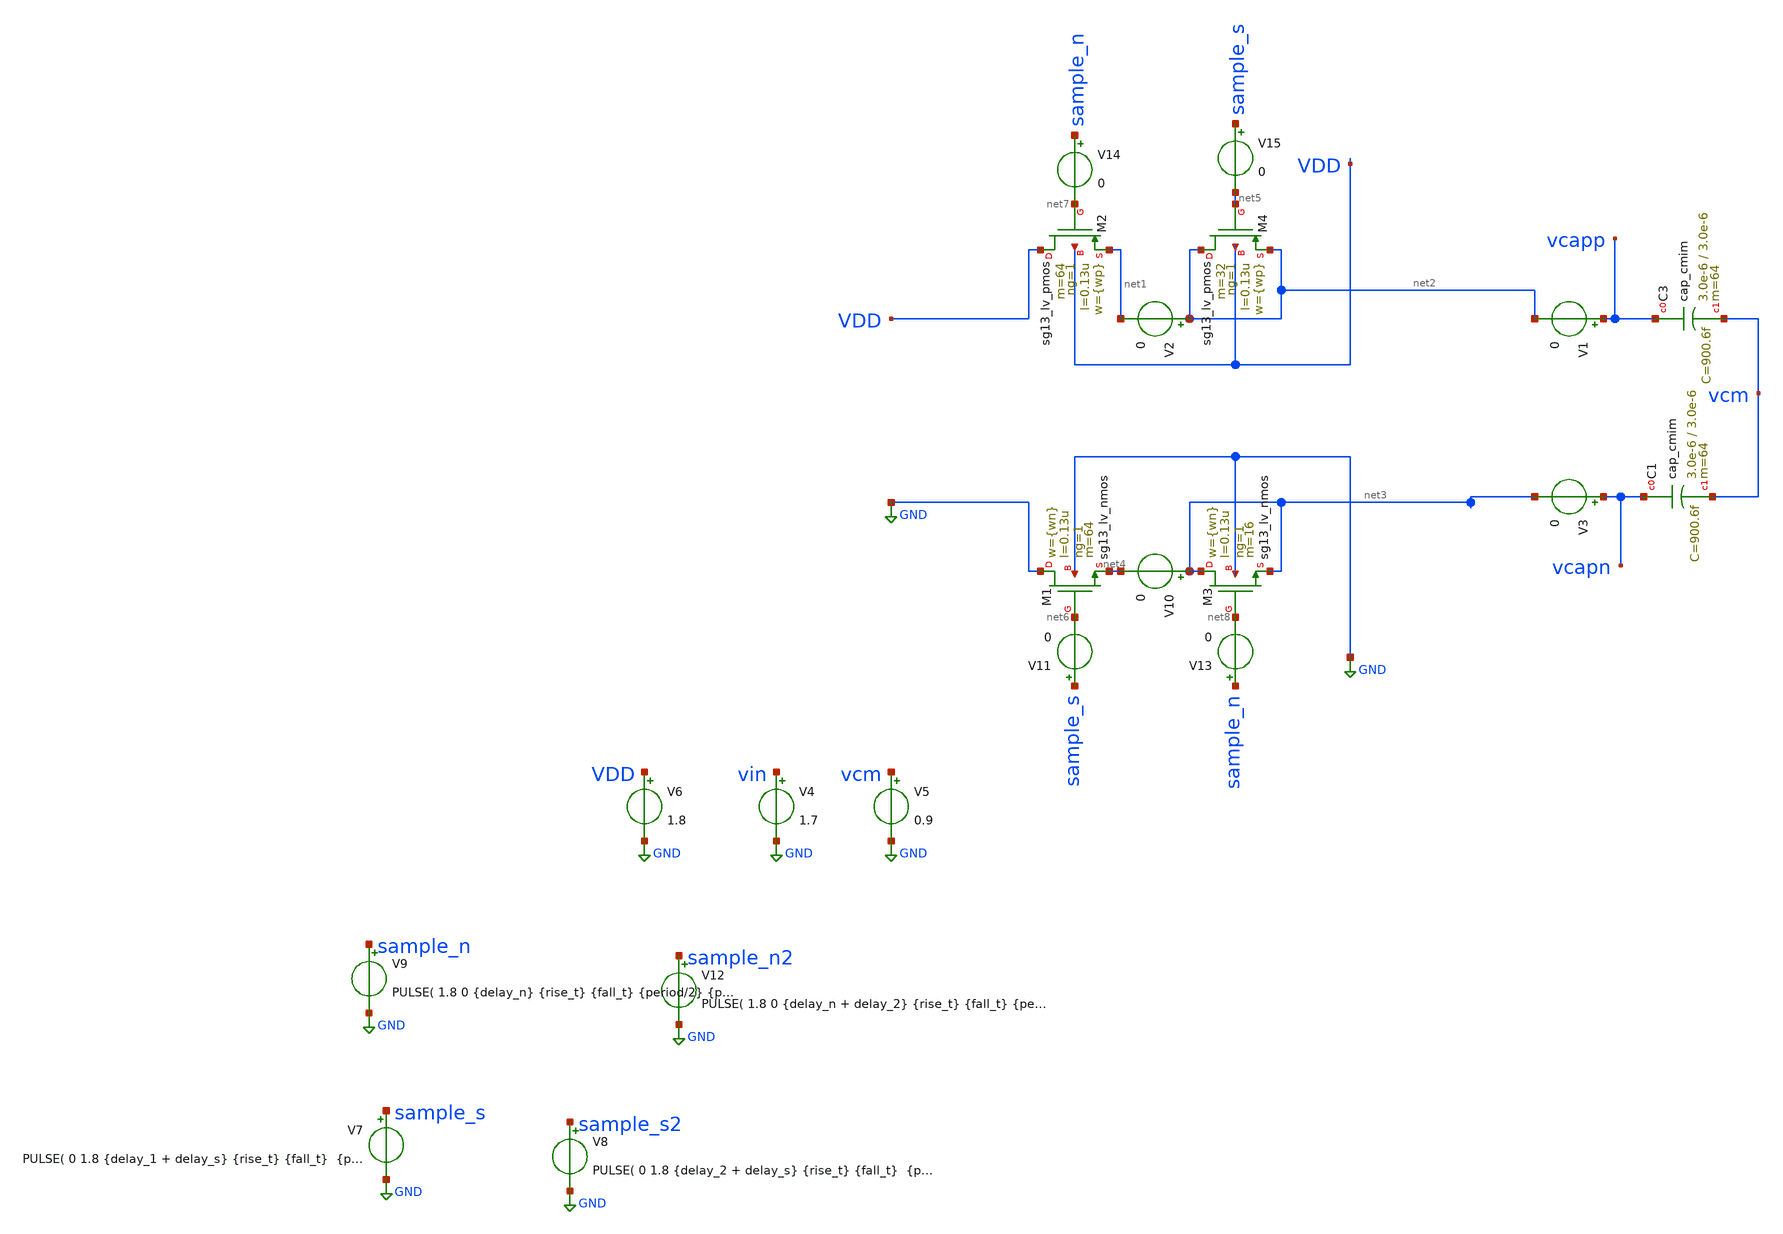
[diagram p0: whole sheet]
** sch_path: xschem/dac_icms_cell/testbenches/tb_dummy.sch
**.subckt tb_dummy
V1 vcapp net2 0
V3 vcapn net3 0
XM1 GND net6 net4 GND sg13_lv_nmos w={wn} l=0.13u ng=1 m=64 mm_ok=1
XM2 VDD net7 net1 VDD sg13_lv_pmos w={wp} l=0.13u ng=1 m=64 mm_ok=1
XM3 net3 net8 net3 GND sg13_lv_nmos w={wn} l=0.13u ng=1 m=16 mm_ok=1
XM4 net2 net5 net2 VDD sg13_lv_pmos w={wp} l=0.13u ng=1 m=32 mm_ok=1
V4 vin GND 1.7
V5 vcm GND 0.9
V6 VDD GND 1.8
V7 sample_s GND PULSE( 0 1.8 {delay_1 + delay_s} {rise_t} {fall_t} {period/2} {period} 1)
V8 sample_s2 GND PULSE( 0 1.8 {delay_2 + delay_s} {rise_t} {fall_t} {period/2} {period} 1)
V9 sample_n GND PULSE( 1.8 0 {delay_n} {rise_t} {fall_t} {period/2} {period} 1)
V12 sample_n2 GND PULSE( 1.8 0 {delay_n + delay_2} {rise_t} {fall_t} {period/2} {period} 1)
V2 net2 net1 0
V10 net3 net4 0
V11 sample_s net6 0
V13 sample_n net8 0
V14 sample_n net7 0
V15 sample_s net5 0
XC3 vcapp vcm cap_cmim w=3.0e-6 l=3.0e-6 m=64 mm_ok=1
XC1 vcapn vcm cap_cmim w=3.0e-6 l=3.0e-6 m=64 mm_ok=1
**** begin user architecture code



.lib cornerMOSlv.lib mos_tt
.lib cornerMOShv.lib mos_tt
.lib cornerHBT.lib hbt_typ
.lib cornerRES.lib res_typ
.lib cornerCAP.lib cap_typ





.param temp=27
.param period = 2n
.param wp = 1.5u
.param wn = 0.5u
.param rise_t = period*0.01
.param fall_t = period*0.01
.param delay_n = 0
.param delay_s = 0
.param delay_2 = period*0.2
.param delay_1 = 0
.options savecurrents klu method=gear reltol=1e-2 abstol=1e-15 gmin=1e-10
.control

* Transient Analysis
tran 1p 2n


plot i(v1) i(v3)
plot sample_s sample_n sample_s2+2 sample_n2+2
plot i(v3)-i(v10) i(v10)
plot i(v1)-i(v2) i(v2)
plot i(v14) i(v15) i(v1)-i(v2) i(v2)

plot i(v11) i(v13) i(v3) i(v10)

plot vcapn vcapp
.endc


**** end user architecture code
**.ends
.GLOBAL GND
.end
